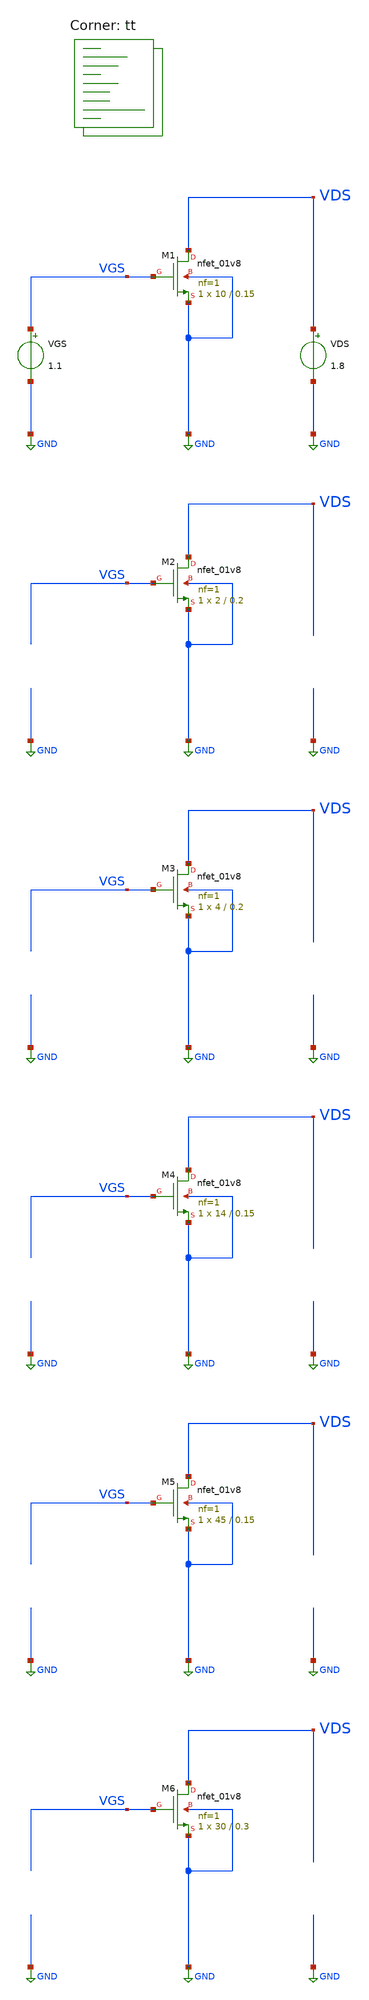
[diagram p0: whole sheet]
** sch_path: projects/opamp/xschem_ngspice/vds_vgs_sweep_nfet.sch
**.subckt vds_vgs_sweep_nfet
XM1 VDS VGS GND GND sky130_fd_pr__nfet_01v8 L=0.15 W=10 nf=1 ad='int((nf+1)/2) * W/nf * 0.29' as='int((nf+2)/2) * W/nf * 0.29'
+ pd='2*int((nf+1)/2) * (W/nf + 0.29)' ps='2*int((nf+2)/2) * (W/nf + 0.29)' nrd='0.29 / W' nrs='0.29 / W'
+ sa=0 sb=0 sd=0 mult=1 m=1
VGS VGS GND 1.1
VDS VDS GND 1.8
XM2 VDS VGS GND GND sky130_fd_pr__nfet_01v8 L=0.2 W=2 nf=1 ad='int((nf+1)/2) * W/nf * 0.29' as='int((nf+2)/2) * W/nf * 0.29'
+ pd='2*int((nf+1)/2) * (W/nf + 0.29)' ps='2*int((nf+2)/2) * (W/nf + 0.29)' nrd='0.29 / W' nrs='0.29 / W'
+ sa=0 sb=0 sd=0 mult=1 m=1
XM3 VDS VGS GND GND sky130_fd_pr__nfet_01v8 L=0.2 W=4 nf=1 ad='int((nf+1)/2) * W/nf * 0.29' as='int((nf+2)/2) * W/nf * 0.29'
+ pd='2*int((nf+1)/2) * (W/nf + 0.29)' ps='2*int((nf+2)/2) * (W/nf + 0.29)' nrd='0.29 / W' nrs='0.29 / W'
+ sa=0 sb=0 sd=0 mult=1 m=1
XM4 VDS VGS GND GND sky130_fd_pr__nfet_01v8 L=0.15 W=14 nf=1 ad='int((nf+1)/2) * W/nf * 0.29' as='int((nf+2)/2) * W/nf * 0.29'
+ pd='2*int((nf+1)/2) * (W/nf + 0.29)' ps='2*int((nf+2)/2) * (W/nf + 0.29)' nrd='0.29 / W' nrs='0.29 / W'
+ sa=0 sb=0 sd=0 mult=1 m=1
XM5 VDS VGS GND GND sky130_fd_pr__nfet_01v8 L=0.15 W=45 nf=1 ad='int((nf+1)/2) * W/nf * 0.29' as='int((nf+2)/2) * W/nf * 0.29'
+ pd='2*int((nf+1)/2) * (W/nf + 0.29)' ps='2*int((nf+2)/2) * (W/nf + 0.29)' nrd='0.29 / W' nrs='0.29 / W'
+ sa=0 sb=0 sd=0 mult=1 m=1
XM6 VDS VGS GND GND sky130_fd_pr__nfet_01v8 L=0.3 W=30 nf=1 ad='int((nf+1)/2) * W/nf * 0.29' as='int((nf+2)/2) * W/nf * 0.29'
+ pd='2*int((nf+1)/2) * (W/nf + 0.29)' ps='2*int((nf+2)/2) * (W/nf + 0.29)' nrd='0.29 / W' nrs='0.29 / W'
+ sa=0 sb=0 sd=0 mult=1 m=1
**** begin user architecture code
.lib $::SKYWATER_MODELS/sky130.lib.spice tt



.option method=gear
.option wnflag=1
.option savecurrents

.save @m.xm1.msky130_fd_pr__nfet_01v8[gm] @m.xm1.msky130_fd_pr__nfet_01v8[gds] @m.xm1.msky130_fd_pr__nfet_01v8[vth] @m.xm2.msky130_fd_pr__nfet_01v8[gm] @m.xm2.msky130_fd_pr__nfet_01v8[gds] @m.xm2.msky130_fd_pr__nfet_01v8[vth] @m.xm3.msky130_fd_pr__nfet_01v8[gm] @m.xm3.msky130_fd_pr__nfet_01v8[gds] @m.xm3.msky130_fd_pr__nfet_01v8[vth] @m.xm4.msky130_fd_pr__nfet_01v8[gm] @m.xm4.msky130_fd_pr__nfet_01v8[gds] @m.xm5.msky130_fd_pr__nfet_01v8[gm] @m.xm5.msky130_fd_pr__nfet_01v8[gds] @m.xm6.msky130_fd_pr__nfet_01v8[gm] @m.xm6.msky130_fd_pr__nfet_01v8[gds] @m.xm7.msky130_fd_pr__nfet_01v8[gm] @m.xm7.msky130_fd_pr__nfet_01v8[gds] @m.xm8.msky130_fd_pr__nfet_01v8[gm] @m.xm8.msky130_fd_pr__nfet_01v8[gds] @m.xm9.msky130_fd_pr__nfet_01v8[gm] @m.xm9.msky130_fd_pr__nfet_01v8[gds] @m.xm10.msky130_fd_pr__nfet_01v8[gm] @m.xm10.msky130_fd_pr__nfet_01v8[gds]


.control
  save all
  * dc VGS 0 1.8 0.001 VDS 0 1.8 0.1
  dc VDS 0 1.4 0.001 VGS 0.2 1.4 0.01
  remzerovec
  write vds_vgs_sweep_nfet.raw
  set appendwrite
  show
.endc



**** end user architecture code
**.ends
.GLOBAL GND
.end
